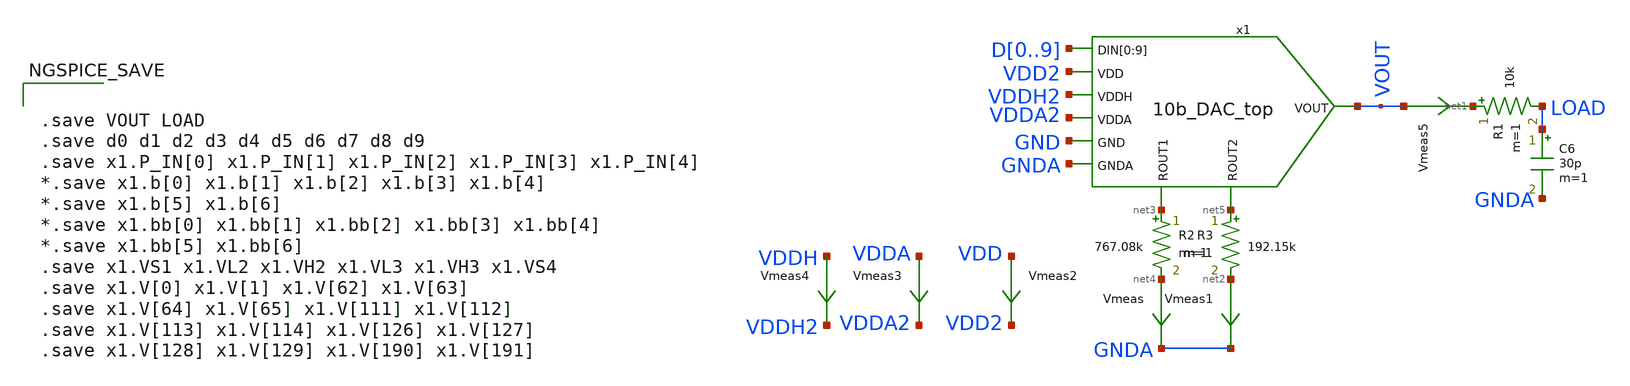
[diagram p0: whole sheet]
** sch_path: xschem/10b_DAC-tb.sch
.lib $::SKYWATER_MODELS/sky130.lib.spice tt
.include $::SKYWATER_STDCELLS/sky130_fd_sc_hd.spice

**.subckt 10b_DAC-tb
C6 LOAD GNDA 30p m=1
R1 net1 LOAD 10k m=1
Vmeas1 net2 GNDA 0
.save i(vmeas1)
R2 net3 net4 767.08k m=1
Vmeas net4 GNDA 0
.save i(vmeas)
R3 net5 net2 192.15k m=1
Vmeas2 VDD VDD2 0
.save i(vmeas2)
x1 D0 D1 D2 D3 D4 D5 D6 D7 D8 D9 VDD2 VDDH2 VDDA2 GND GNDA VOUT net3 net5 10b_DAC_top
Vmeas3 VDDA VDDA2 0
.save i(vmeas3)
Vmeas4 VDDH VDDH2 0
.save i(vmeas4)
Vmeas5 VOUT net1 0
.save i(vmeas5)
**** begin user architecture code



  *.options wnflag=0 bypass=1
  .option wnflag=1
  .option safecurrents
  *.option klu
  .options solver=klu nomod
  .options method=trap rawfile=binary
  *.options reltol=1e-2 abstol=1e-12 chgtol=1e-14
  ********************Static Voltage Sources***************************
  Vddh vddh gnd dc 5.5
  Vdd vdd gnd dc 1.8
  Vdda vdda gnd dc 5.5
  Vgnda gnda gnd dc 0

  VHREF x1.V[191] GND 5.5
  VLREF x1.V[0] GND 0
  ********************Dynamic Voltage Sources***************************
  *******Calculation**********
  .param base_f=100e3 base_t={1/base_f} base_th={base_t/2} base_d={base_th}
  .param d0_th={base_th} d0_t={d0_th*2}
  .param d1_th={d0_th*2} d1_t={d1_th*2}
  .param d2_th={d1_th*2} d2_t={d2_th*2}
  .param d3_th={d2_th*2} d3_t={d3_th*2}
  .param d4_th={d3_th*2} d4_t={d4_th*2}
  .param d5_th={d4_th*2} d5_t={d5_th*2}
  .param d6_th={d5_th*2} d6_t={d6_th*2}
  .param d7_th={d6_th*2} d7_t={d7_th*2}
  .param d8_th={d7_th*2} d8_t={d8_th*2}
  .param d9_th={d8_th*2} d9_t={d9_th*2}
  *******Signals**********
  .param vhi=1.8

  *Bd5  d5  gnd V = {V(in) - 64*LSB0*floor(V(in)/(64*LSB0)) >= 32*LSB0 ? 1.8 : 0}
  *Bd6  d6  gnd V = {V(in) - 128*LSB0*floor(V(in)/(128*LSB0)) >= 64*LSB0 ? 1.8 : 0}
  *Bd7  d7  gnd V = {V(in) - 256*LSB0*floor(V(in)/(256*LSB0)) >= 128*LSB0 ? 1.8 : 0}
  *Bd8  d8  gnd V = {V(in) - 512*LSB0*floor(V(in)/(512*LSB0)) >= 256*LSB0 ? 1.8 : 0}
  *Bd9  d9  gnd V = {V(in) - 1024*LSB0*floor(V(in)/(1024*LSB0)) >= 512*LSB0 ? 1.8 : 0}

  Vd0  d0  gnd pulse({vhi} 0 {base_d} 1n 1n {d0_th} {d0_t})
  Vd1  d1  gnd pulse({vhi} 0 {base_d} 1n 1n {d1_th} {d1_t})
  Vd2  d2  gnd pulse({vhi} 0 {base_d} 1n 1n {d2_th} {d2_t})
  Vd3  d3  gnd pulse({vhi} 0 {base_d} 1n 1n {d3_th} {d3_t})
  Vd4  d4  gnd pulse({vhi} 0 {base_d} 1n 1n {d4_th} {d4_t})

  *Bd5  d5  gnd V = {V(in) - 64*LSB0*floor(V(in)/(64*LSB0)) >= 32*LSB0 ? 1.8 : 0}
  *Bd6  d6  gnd V = {V(in) - 128*LSB0*floor(V(in)/(128*LSB0)) >= 64*LSB0 ? 1.8 : 0}
  *Bd7  d7  gnd V = {V(in) - 256*LSB0*floor(V(in)/(256*LSB0)) >= 128*LSB0 ? 1.8 : 0}
  *Bd8  d8  gnd V = {V(in) - 512*LSB0*floor(V(in)/(512*LSB0)) >= 256*LSB0 ? 1.8 : 0}
  *Bd9  d9  gnd V = {V(in) - 1024*LSB0*floor(V(in)/(1024*LSB0)) >= 512*LSB0 ? 1.8 : 0}

  *Vd5  d5  gnd pulse({vhi} 0 {base_d} 1n 1n {d5_th} {d5_t})
  *Vd6  d6  gnd pulse({vhi} 0 {base_d} 1n 1n {d6_th} {d6_t})
  *Vd7  d7  gnd pulse({vhi} 0 {base_d} 1n 1n {d7_th} {d7_t})
  *Vd8  d8  gnd pulse({vhi} 0 {base_d} 1n 1n {d8_th} {d8_t})
  *Vd9  d9  gnd pulse({vhi} 0 {base_d} 1n 1n {d9_th} {d9_t})

  Vd5  d5  gnd 0
  Vd6  d6  gnd 0
  Vd7  d7  gnd 0
  Vd8  d8  gnd 0
  Vd9  d9  gnd 0
  ********************Simulation Commands*****************************
  .tran 1n 170u
  .control
     reset
     set wr_vecnames
     set wr_singlescale
     set num_threads=16
     *let iterration=0


     compose low_to_high values 0 1.8
     compose high_to_low values 1.8 0

     foreach var9 $&low_to_high
       alter vd9 $var9

       foreach var8 $&low_to_high
         alter vd8 $var8

         foreach var7 $&low_to_high
           alter vd7 $var7

             foreach var6 $&low_to_high
             alter vd6 $var6

             foreach var5 $&low_to_high
             alter vd5 $var5

             run
             write top_step_tr-tb.raw

             let voutval= v(vout)
             let vloadval = v(load)

             let ir1 = i(vmeas)
             let ir2 = i(vmeas1)
             let ivdd = i(vmeas2)
             let ivdda = i(vmeas3)
             let ivddh = i(vmeas4)

             let vd0 = v(d0)
             let vd1 = v(d1)
             let vd2 = v(d2)
             let vd3 = v(d3)
             let vd4 = v(d4)
             let vd5 = v(d5)
             let vd6 = v(d6)
             let vd7 = v(d7)
             let vd8 = v(d8)
             let vd9 = v(d9)

             wrdata $THESIS_WS/simulations/top_step_tr-tb.txt voutval vloadval ir1 ir2 ivdd ivdda
+ ivddh vd9 vd8 vd7 vd6 vd5 vd4 vd3 vd2 vd1 vd0
             *let iterration = iterration + 1
             set appendwrite
             unset set wr_vecnames
             destroy all
          end
          end
          end
          end
          end

*    quit 0
  .endc





.save VOUT LOAD
.save d0 d1 d2 d3 d4 d5 d6 d7 d8 d9
.save x1.P_IN[0] x1.P_IN[1] x1.P_IN[2] x1.P_IN[3] x1.P_IN[4]
*.save x1.b[0] x1.b[1] x1.b[2] x1.b[3] x1.b[4]
*.save x1.b[5] x1.b[6]
*.save x1.bb[0] x1.bb[1] x1.bb[2] x1.bb[3] x1.bb[4]
*.save x1.bb[5] x1.bb[6]
.save x1.VS1 x1.VL2 x1.VH2 x1.VL3 x1.VH3 x1.VS4
.save x1.V[0] x1.V[1] x1.V[62] x1.V[63]
.save x1.V[64] x1.V[65] x1.V[111] x1.V[112]
.save x1.V[113] x1.V[114] x1.V[126] x1.V[127]
.save x1.V[128] x1.V[129] x1.V[190] x1.V[191]


**** end user architecture code
**.ends
.end
